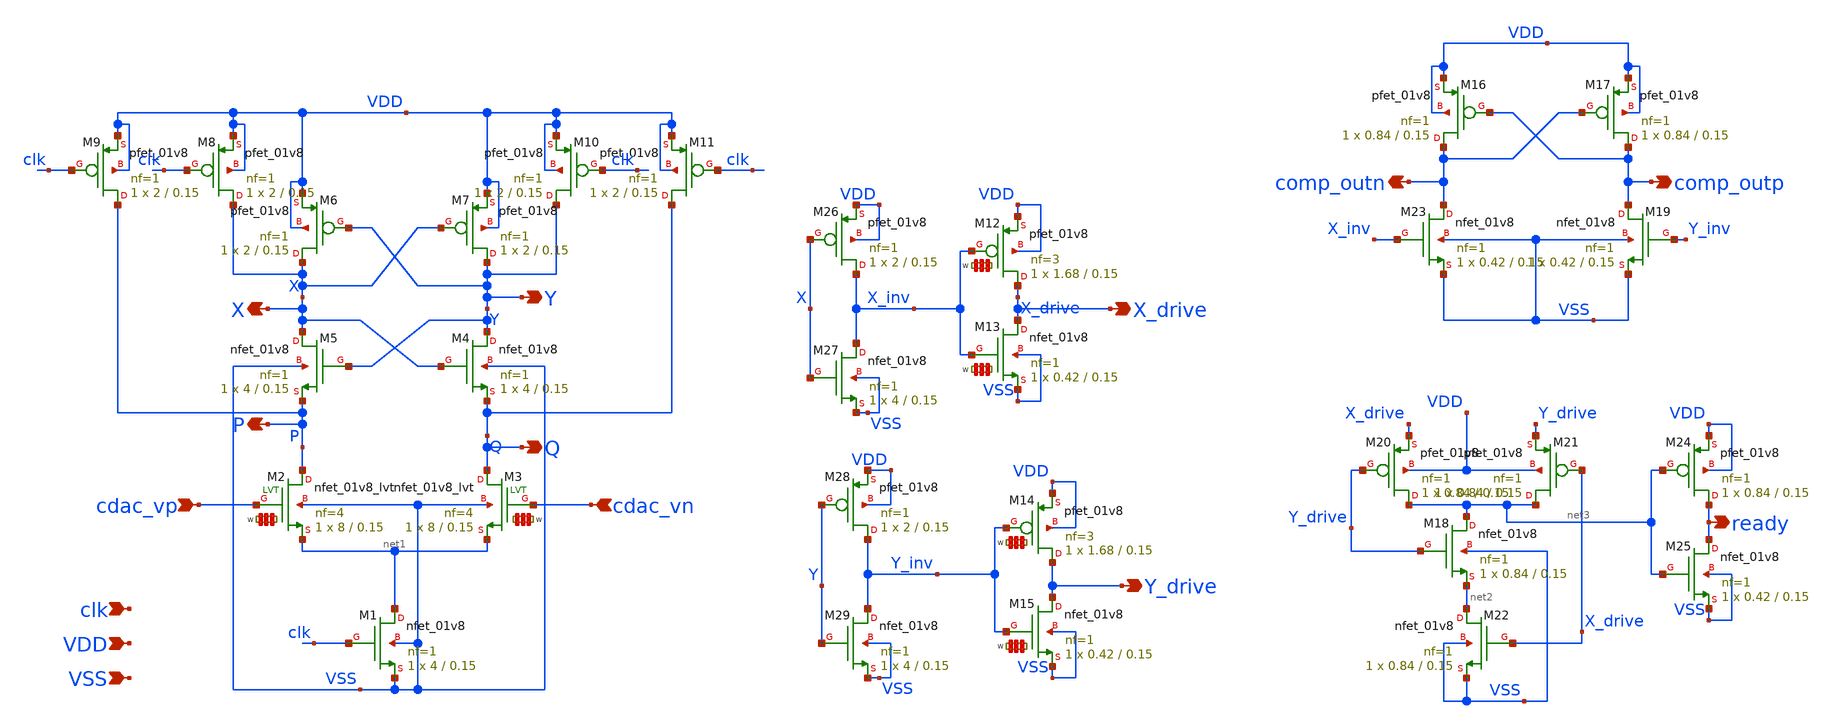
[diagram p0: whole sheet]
** sch_path: module/comparator/comp.sch
**.subckt comp cdac_vn cdac_vp VSS VDD comp_outn comp_outp ready clk X Y P Q X_drive Y_drive
*.ipin cdac_vn
*.ipin cdac_vp
*.ipin VSS
*.ipin VDD
*.opin comp_outn
*.opin comp_outp
*.opin ready
*.ipin clk
*.opin X
*.opin Y
*.opin P
*.opin Q
*.opin X_drive
*.opin Y_drive
XM1 net1 clk VSS VSS sky130_fd_pr__nfet_01v8 L=0.15 W=4 nf=1 ad='int((nf+1)/2) * W/nf * 0.29' as='int((nf+2)/2) * W/nf * 0.29'
+ pd='2*int((nf+1)/2) * (W/nf + 0.29)' ps='2*int((nf+2)/2) * (W/nf + 0.29)' nrd='0.29 / W' nrs='0.29 / W'
+ sa=0 sb=0 sd=0 mult=1 m=1
XM4 Y X Q VSS sky130_fd_pr__nfet_01v8 L=0.15 W=4 nf=1 ad='int((nf+1)/2) * W/nf * 0.29' as='int((nf+2)/2) * W/nf * 0.29'
+ pd='2*int((nf+1)/2) * (W/nf + 0.29)' ps='2*int((nf+2)/2) * (W/nf + 0.29)' nrd='0.29 / W' nrs='0.29 / W'
+ sa=0 sb=0 sd=0 mult=1 m=1
XM5 X Y P VSS sky130_fd_pr__nfet_01v8 L=0.15 W=4 nf=1 ad='int((nf+1)/2) * W/nf * 0.29' as='int((nf+2)/2) * W/nf * 0.29'
+ pd='2*int((nf+1)/2) * (W/nf + 0.29)' ps='2*int((nf+2)/2) * (W/nf + 0.29)' nrd='0.29 / W' nrs='0.29 / W'
+ sa=0 sb=0 sd=0 mult=1 m=1
XM6 X Y VDD VDD sky130_fd_pr__pfet_01v8 L=0.15 W=2 nf=1 ad='int((nf+1)/2) * W/nf * 0.29' as='int((nf+2)/2) * W/nf * 0.29'
+ pd='2*int((nf+1)/2) * (W/nf + 0.29)' ps='2*int((nf+2)/2) * (W/nf + 0.29)' nrd='0.29 / W' nrs='0.29 / W'
+ sa=0 sb=0 sd=0 mult=1 m=1
XM7 Y X VDD VDD sky130_fd_pr__pfet_01v8 L=0.15 W=2 nf=1 ad='int((nf+1)/2) * W/nf * 0.29' as='int((nf+2)/2) * W/nf * 0.29'
+ pd='2*int((nf+1)/2) * (W/nf + 0.29)' ps='2*int((nf+2)/2) * (W/nf + 0.29)' nrd='0.29 / W' nrs='0.29 / W'
+ sa=0 sb=0 sd=0 mult=1 m=1
XM8 X clk VDD VDD sky130_fd_pr__pfet_01v8 L=0.15 W=2 nf=1 ad='int((nf+1)/2) * W/nf * 0.29' as='int((nf+2)/2) * W/nf * 0.29'
+ pd='2*int((nf+1)/2) * (W/nf + 0.29)' ps='2*int((nf+2)/2) * (W/nf + 0.29)' nrd='0.29 / W' nrs='0.29 / W'
+ sa=0 sb=0 sd=0 mult=1 m=1
XM9 P clk VDD VDD sky130_fd_pr__pfet_01v8 L=0.15 W=2 nf=1 ad='int((nf+1)/2) * W/nf * 0.29' as='int((nf+2)/2) * W/nf * 0.29'
+ pd='2*int((nf+1)/2) * (W/nf + 0.29)' ps='2*int((nf+2)/2) * (W/nf + 0.29)' nrd='0.29 / W' nrs='0.29 / W'
+ sa=0 sb=0 sd=0 mult=1 m=1
XM10 Y clk VDD VDD sky130_fd_pr__pfet_01v8 L=0.15 W=2 nf=1 ad='int((nf+1)/2) * W/nf * 0.29' as='int((nf+2)/2) * W/nf * 0.29'
+ pd='2*int((nf+1)/2) * (W/nf + 0.29)' ps='2*int((nf+2)/2) * (W/nf + 0.29)' nrd='0.29 / W' nrs='0.29 / W'
+ sa=0 sb=0 sd=0 mult=1 m=1
XM11 Q clk VDD VDD sky130_fd_pr__pfet_01v8 L=0.15 W=2 nf=1 ad='int((nf+1)/2) * W/nf * 0.29' as='int((nf+2)/2) * W/nf * 0.29'
+ pd='2*int((nf+1)/2) * (W/nf + 0.29)' ps='2*int((nf+2)/2) * (W/nf + 0.29)' nrd='0.29 / W' nrs='0.29 / W'
+ sa=0 sb=0 sd=0 mult=1 m=1
XM16 comp_outn comp_outp VDD VDD sky130_fd_pr__pfet_01v8 L=0.15 W=0.84 nf=1 ad='int((nf+1)/2) * W/nf * 0.29'
+ as='int((nf+2)/2) * W/nf * 0.29' pd='2*int((nf+1)/2) * (W/nf + 0.29)' ps='2*int((nf+2)/2) * (W/nf + 0.29)'
+ nrd='0.29 / W' nrs='0.29 / W' sa=0 sb=0 sd=0 mult=1 m=1
XM17 comp_outp comp_outn VDD VDD sky130_fd_pr__pfet_01v8 L=0.15 W=0.84 nf=1 ad='int((nf+1)/2) * W/nf * 0.29'
+ as='int((nf+2)/2) * W/nf * 0.29' pd='2*int((nf+1)/2) * (W/nf + 0.29)' ps='2*int((nf+2)/2) * (W/nf + 0.29)'
+ nrd='0.29 / W' nrs='0.29 / W' sa=0 sb=0 sd=0 mult=1 m=1
XM18 net3 Y_drive net2 VSS sky130_fd_pr__nfet_01v8 L=0.15 W=0.84 nf=1 ad='int((nf+1)/2) * W/nf * 0.29'
+ as='int((nf+2)/2) * W/nf * 0.29' pd='2*int((nf+1)/2) * (W/nf + 0.29)' ps='2*int((nf+2)/2) * (W/nf + 0.29)'
+ nrd='0.29 / W' nrs='0.29 / W' sa=0 sb=0 sd=0 mult=1 m=1
XM19 comp_outp Y_inv VSS VSS sky130_fd_pr__nfet_01v8 L=0.15 W=0.42 nf=1 ad='int((nf+1)/2) * W/nf * 0.29'
+ as='int((nf+2)/2) * W/nf * 0.29' pd='2*int((nf+1)/2) * (W/nf + 0.29)' ps='2*int((nf+2)/2) * (W/nf + 0.29)'
+ nrd='0.29 / W' nrs='0.29 / W' sa=0 sb=0 sd=0 mult=1 m=1
XM20 net3 Y_drive X_drive VDD sky130_fd_pr__pfet_01v8 L=0.15 W=0.84 nf=1 ad='int((nf+1)/2) * W/nf * 0.29'
+ as='int((nf+2)/2) * W/nf * 0.29' pd='2*int((nf+1)/2) * (W/nf + 0.29)' ps='2*int((nf+2)/2) * (W/nf + 0.29)'
+ nrd='0.29 / W' nrs='0.29 / W' sa=0 sb=0 sd=0 mult=1 m=1
XM21 net3 X_drive Y_drive VDD sky130_fd_pr__pfet_01v8 L=0.15 W=0.84 nf=1 ad='int((nf+1)/2) * W/nf * 0.29'
+ as='int((nf+2)/2) * W/nf * 0.29' pd='2*int((nf+1)/2) * (W/nf + 0.29)' ps='2*int((nf+2)/2) * (W/nf + 0.29)'
+ nrd='0.29 / W' nrs='0.29 / W' sa=0 sb=0 sd=0 mult=1 m=1
XM22 net2 X_drive VSS VSS sky130_fd_pr__nfet_01v8 L=0.15 W=0.84 nf=1 ad='int((nf+1)/2) * W/nf * 0.29'
+ as='int((nf+2)/2) * W/nf * 0.29' pd='2*int((nf+1)/2) * (W/nf + 0.29)' ps='2*int((nf+2)/2) * (W/nf + 0.29)'
+ nrd='0.29 / W' nrs='0.29 / W' sa=0 sb=0 sd=0 mult=1 m=1
XM23 comp_outn X_inv VSS VSS sky130_fd_pr__nfet_01v8 L=0.15 W=0.42 nf=1 ad='int((nf+1)/2) * W/nf * 0.29'
+ as='int((nf+2)/2) * W/nf * 0.29' pd='2*int((nf+1)/2) * (W/nf + 0.29)' ps='2*int((nf+2)/2) * (W/nf + 0.29)'
+ nrd='0.29 / W' nrs='0.29 / W' sa=0 sb=0 sd=0 mult=1 m=1
XM24 ready net3 VDD VDD sky130_fd_pr__pfet_01v8 L=0.15 W=0.84 nf=1 ad='int((nf+1)/2) * W/nf * 0.29' as='int((nf+2)/2) * W/nf * 0.29'
+ pd='2*int((nf+1)/2) * (W/nf + 0.29)' ps='2*int((nf+2)/2) * (W/nf + 0.29)' nrd='0.29 / W' nrs='0.29 / W'
+ sa=0 sb=0 sd=0 mult=1 m=1
XM25 ready net3 VSS VSS sky130_fd_pr__nfet_01v8 L=0.15 W=0.42 nf=1 ad='int((nf+1)/2) * W/nf * 0.29' as='int((nf+2)/2) * W/nf * 0.29'
+ pd='2*int((nf+1)/2) * (W/nf + 0.29)' ps='2*int((nf+2)/2) * (W/nf + 0.29)' nrd='0.29 / W' nrs='0.29 / W'
+ sa=0 sb=0 sd=0 mult=1 m=1
XM12 X_drive X_inv VDD VDD sky130_fd_pr__pfet_01v8 L=0.15 W='1.68 * 3 ' nf=3 ad='int((nf+1)/2) * W / nf * 0.29'
+ as='int((nf+2)/2) * W / nf * 0.29' pd='2*int((nf+1)/2) * (W / nf + 0.29)' ps='2*int((nf+2)/2) * (W / nf + 0.29)'
+ nrd='0.29 / W ' nrs='0.29 / W ' sa=0 sb=0 sd=0 mult=1 m=1
XM13 X_drive X_inv VSS VSS sky130_fd_pr__nfet_01v8 L=0.15 W='0.42 * 1 ' nf=1 ad='int((nf+1)/2) * W / nf * 0.29'
+ as='int((nf+2)/2) * W / nf * 0.29' pd='2*int((nf+1)/2) * (W / nf + 0.29)' ps='2*int((nf+2)/2) * (W / nf + 0.29)'
+ nrd='0.29 / W ' nrs='0.29 / W ' sa=0 sb=0 sd=0 mult=1 m=1
XM14 Y_drive Y_inv VDD VDD sky130_fd_pr__pfet_01v8 L=0.15 W='1.68 * 3 ' nf=3 ad='int((nf+1)/2) * W / nf * 0.29'
+ as='int((nf+2)/2) * W / nf * 0.29' pd='2*int((nf+1)/2) * (W / nf + 0.29)' ps='2*int((nf+2)/2) * (W / nf + 0.29)'
+ nrd='0.29 / W ' nrs='0.29 / W ' sa=0 sb=0 sd=0 mult=1 m=1
XM15 Y_drive Y_inv VSS VSS sky130_fd_pr__nfet_01v8 L=0.15 W='0.42 * 1 ' nf=1 ad='int((nf+1)/2) * W / nf * 0.29'
+ as='int((nf+2)/2) * W / nf * 0.29' pd='2*int((nf+1)/2) * (W / nf + 0.29)' ps='2*int((nf+2)/2) * (W / nf + 0.29)'
+ nrd='0.29 / W ' nrs='0.29 / W ' sa=0 sb=0 sd=0 mult=1 m=1
XM2 P cdac_vp net1 VSS sky130_fd_pr__nfet_01v8_lvt L=0.15 W='8 * 4 ' nf=4 ad='int((nf+1)/2) * W / nf * 0.29'
+ as='int((nf+2)/2) * W / nf * 0.29' pd='2*int((nf+1)/2) * (W / nf + 0.29)' ps='2*int((nf+2)/2) * (W / nf + 0.29)'
+ nrd='0.29 / W ' nrs='0.29 / W ' sa=0 sb=0 sd=0 mult=1 m=1
XM3 Q cdac_vn net1 VSS sky130_fd_pr__nfet_01v8_lvt L=0.15 W='8 * 4 ' nf=4 ad='int((nf+1)/2) * W / nf * 0.29'
+ as='int((nf+2)/2) * W / nf * 0.29' pd='2*int((nf+1)/2) * (W / nf + 0.29)' ps='2*int((nf+2)/2) * (W / nf + 0.29)'
+ nrd='0.29 / W ' nrs='0.29 / W ' sa=0 sb=0 sd=0 mult=1 m=1
XM26 X_inv X VDD VDD sky130_fd_pr__pfet_01v8 L=0.15 W=2 nf=1 ad='int((nf+1)/2) * W/nf * 0.29' as='int((nf+2)/2) * W/nf * 0.29'
+ pd='2*int((nf+1)/2) * (W/nf + 0.29)' ps='2*int((nf+2)/2) * (W/nf + 0.29)' nrd='0.29 / W' nrs='0.29 / W'
+ sa=0 sb=0 sd=0 mult=1 m=1
XM27 X_inv X VSS VSS sky130_fd_pr__nfet_01v8 L=0.15 W=4 nf=1 ad='int((nf+1)/2) * W/nf * 0.29' as='int((nf+2)/2) * W/nf * 0.29'
+ pd='2*int((nf+1)/2) * (W/nf + 0.29)' ps='2*int((nf+2)/2) * (W/nf + 0.29)' nrd='0.29 / W' nrs='0.29 / W'
+ sa=0 sb=0 sd=0 mult=1 m=1
XM28 Y_inv Y VDD VDD sky130_fd_pr__pfet_01v8 L=0.15 W=2 nf=1 ad='int((nf+1)/2) * W/nf * 0.29' as='int((nf+2)/2) * W/nf * 0.29'
+ pd='2*int((nf+1)/2) * (W/nf + 0.29)' ps='2*int((nf+2)/2) * (W/nf + 0.29)' nrd='0.29 / W' nrs='0.29 / W'
+ sa=0 sb=0 sd=0 mult=1 m=1
XM29 Y_inv Y VSS VSS sky130_fd_pr__nfet_01v8 L=0.15 W=4 nf=1 ad='int((nf+1)/2) * W/nf * 0.29' as='int((nf+2)/2) * W/nf * 0.29'
+ pd='2*int((nf+1)/2) * (W/nf + 0.29)' ps='2*int((nf+2)/2) * (W/nf + 0.29)' nrd='0.29 / W' nrs='0.29 / W'
+ sa=0 sb=0 sd=0 mult=1 m=1
**.ends
.end
